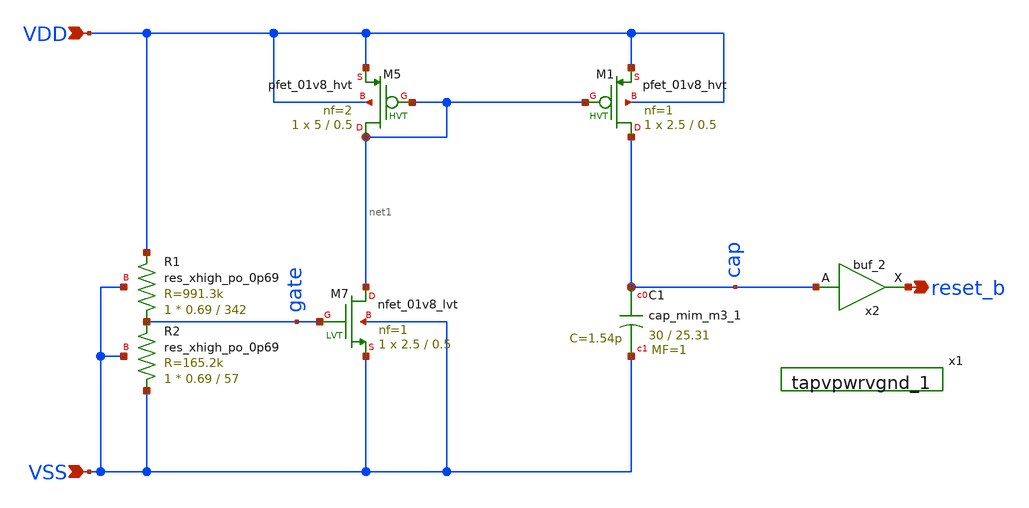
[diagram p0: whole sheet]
** sch_path: xschem/single_stage_por.sch
**.subckt single_stage_por VDD VSS reset_b
*.ipin VDD
*.ipin VSS
*.opin reset_b
XM5 net1 net1 VDD VDD sky130_fd_pr__pfet_01v8_hvt L=0.5 W=5 nf=2 ad='int((nf+1)/2) * W/nf * 0.29' as='int((nf+2)/2) * W/nf * 0.29'
+ pd='2*int((nf+1)/2) * (W/nf + 0.29)' ps='2*int((nf+2)/2) * (W/nf + 0.29)' nrd='0.29 / W' nrs='0.29 / W'
+ sa=0 sb=0 sd=0 mult=1 m=1
XM7 net1 gate VSS VSS sky130_fd_pr__nfet_01v8_lvt L=0.5 W=2.5 nf=1 ad='int((nf+1)/2) * W/nf * 0.29' as='int((nf+2)/2) * W/nf * 0.29'
+ pd='2*int((nf+1)/2) * (W/nf + 0.29)' ps='2*int((nf+2)/2) * (W/nf + 0.29)' nrd='0.29 / W' nrs='0.29 / W'
+ sa=0 sb=0 sd=0 mult=1 m=1
XR1 gate VDD VSS sky130_fd_pr__res_xhigh_po_0p69 L=342 mult=1 m=1
XR2 VSS gate VSS sky130_fd_pr__res_xhigh_po_0p69 L=57 mult=1 m=1
XM1 cap net1 VDD VDD sky130_fd_pr__pfet_01v8_hvt L=0.5 W=2.5 nf=1 ad='int((nf+1)/2) * W/nf * 0.29' as='int((nf+2)/2) * W/nf * 0.29'
+ pd='2*int((nf+1)/2) * (W/nf + 0.29)' ps='2*int((nf+2)/2) * (W/nf + 0.29)' nrd='0.29 / W' nrs='0.29 / W'
+ sa=0 sb=0 sd=0 mult=1 m=1
XC1 cap VSS sky130_fd_pr__cap_mim_m3_1 W=30 L=25.31 MF=1 m=1
x2 cap VSS VSS VDD VDD reset_b sky130_fd_sc_hd__buf_2
x1 vss vdd sky130_fd_sc_hd__tapvpwrvgnd_1
**.ends
.end
